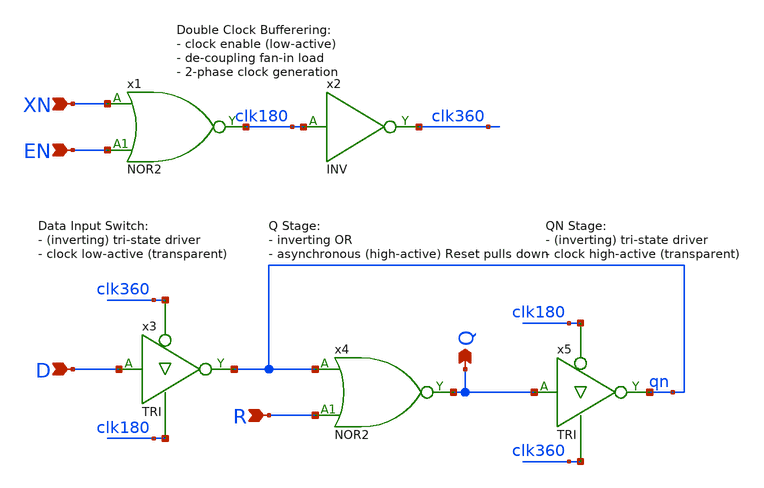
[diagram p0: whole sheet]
** sch_path: Sources/crafted/LATNER.sch
**.subckt LATNER XN D Q EN R
*.ipin XN
*.ipin D
*.opin Q
*.ipin EN
*.ipin R
x1 XN EN clk180 VDD GND NOR2 Wmin=1.5u Lmin=1u g=2 m=1
x2 clk180 clk360 VDD GND INV Wmin=1.5u Lmin=1u g=2 m=1
x3 D clk360 clk180 qn VDD GND TRI Wmin=1.5u Lmin=1u g=2 m=1
x4 qn R Q VDD GND NOR2 Wmin=1.5u Lmin=1u g=2 m=1
x5 Q clk180 clk360 qn VDD GND TRI Wmin=1.5u Lmin=1u g=2 m=1
**.ends
.end
